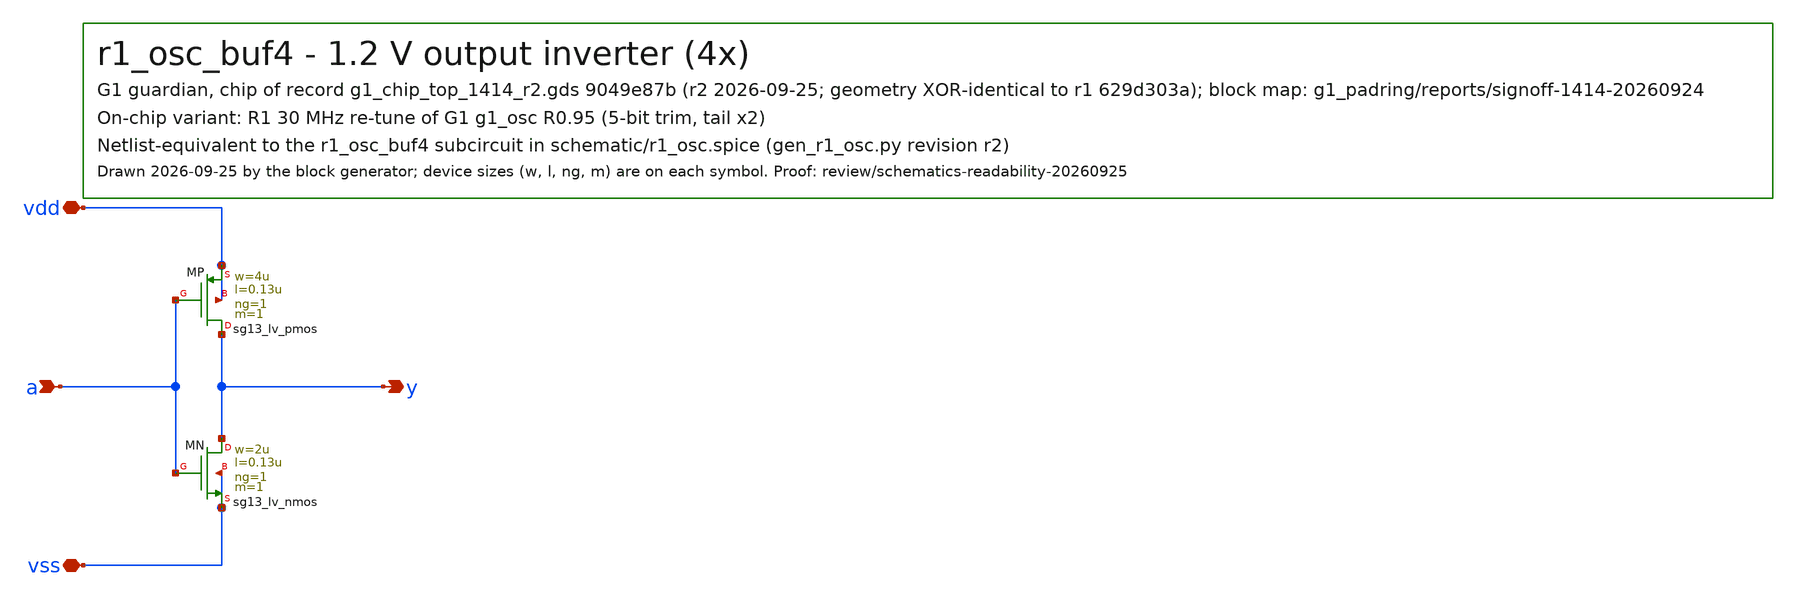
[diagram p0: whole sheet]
** sch_path: designs/r1-joint/blocks/r1_osc/schematic/r1_osc_buf4.sch
**.subckt r1_osc_buf4 a y vdd vss
*.ipin a
*.opin y
*.iopin vdd
*.iopin vss
XMP y a vdd vdd sg13_lv_pmos w=4u l=0.13u ng=1 m=1 mm_ok=1
XMN y a vss vss sg13_lv_nmos w=2u l=0.13u ng=1 m=1 mm_ok=1
**.ends
.end
